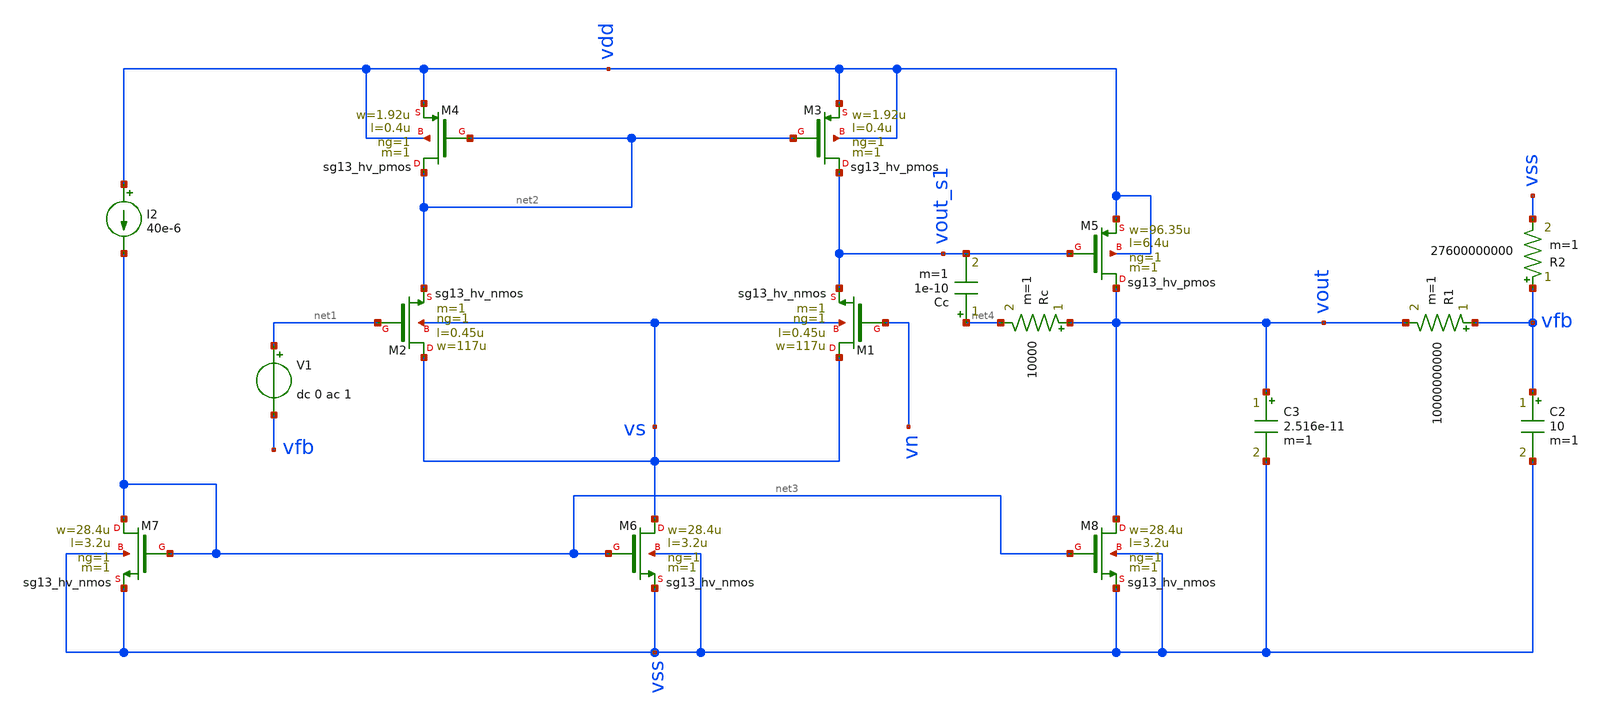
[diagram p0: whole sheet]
** sch_path: test/Tesis_notebooks/xschem/ota_2stage_tb.sch
**.subckt ota_2stage_tb
XM1 vs vn vout_s1 vs sg13_hv_nmos w=117u l=0.45u ng=1 m=1 mm_ok=1
XM2 vs net1 net2 vs sg13_hv_nmos w=117u l=0.45u ng=1 m=1 mm_ok=1
XM3 vout_s1 net2 vdd vdd sg13_hv_pmos w=1.92u l=0.4u ng=1 m=1 mm_ok=1
XM4 net2 net2 vdd vdd sg13_hv_pmos w=1.92u l=0.4u ng=1 m=1 mm_ok=1
XM5 vout vout_s1 vdd vdd sg13_hv_pmos w=96.35u l=6.4u ng=1 m=1 mm_ok=1
R1 vfb vout 10000000000 m=1
C2 vfb vss 10 m=1
R2 vfb vss 27600000000 m=1
V1 net1 vfb dc 0 ac 1
C3 vout vss 2.516e-11 m=1
XM6 vs net3 vss vss sg13_hv_nmos w=28.4u l=3.2u ng=1 m=1 mm_ok=1
XM7 net3 net3 vss vss sg13_hv_nmos w=28.4u l=3.2u ng=1 m=1 mm_ok=1
I2 vdd net3 40e-6
XM8 vout net3 vss vss sg13_hv_nmos w=28.4u l=3.2u ng=1 m=1 mm_ok=1
Cc net4 vout_s1 1e-10 m=1
Rc vout net4 10000 m=1
**** begin user architecture code



.lib /opt/pdks/ihp-sg13g2/libs.tech/ngspice/models/cornerMOShv.lib mos_tt

Vref vn 0 0.9
Vdd vdd 0 1.8
Vss vss 0 0

.control
ac dec 10 1 1G
plot vdb(vout)
plot phase(vout)*180/PI
meas pm find phase(vout)*180/PI when vdb(vout)=0
op
print vout vs vout_s1 vfb
.endc



**** end user architecture code
**.ends
.end
